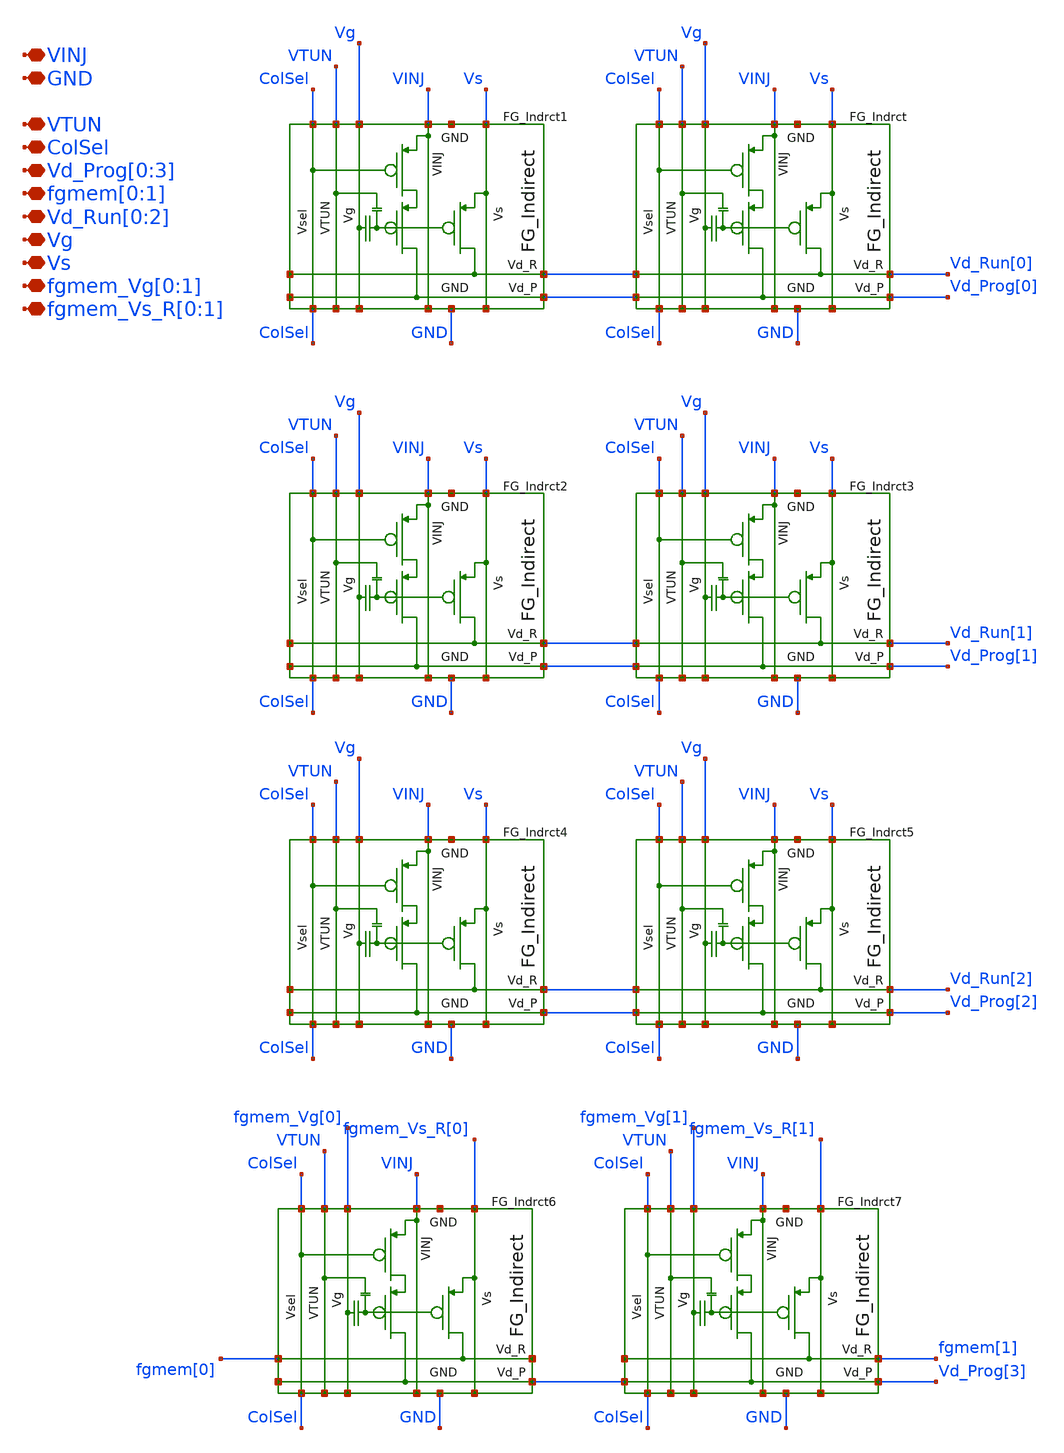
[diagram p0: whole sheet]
** sch_path: sky130_cells/IndirectVMM_Bot_Bmat_4x2/IndirectVMM_Bot_Bmat_4x2.sch
**.subckt IndirectVMM_Bot_Bmat_4x2 Vd_Run[0],Vd_Run[1],Vd_Run[2]
*+ Vd_Prog[0],Vd_Prog[1],Vd_Prog[2],Vd_Prog[3] Vg VTUN ColSel GND VINJ Vs fgmem[0],fgmem[1] fgmem_Vg[0],fgmem_Vg[1] fgmem_Vs_R[0],fgmem_Vs_R[1]
*.iopin Vd_Run[0],Vd_Run[1],Vd_Run[2]
*.iopin Vd_Prog[0],Vd_Prog[1],Vd_Prog[2],Vd_Prog[3]
*.iopin Vg
*.iopin VTUN
*.iopin ColSel
*.iopin GND
*.iopin VINJ
*.iopin Vs
*.iopin fgmem[0],fgmem[1]
*.iopin fgmem_Vg[0],fgmem_Vg[1]
*.iopin fgmem_Vs_R[0],fgmem_Vs_R[1]
FG_Indrct1 Vs Vg ColSel VTUN Vd_Run[0] Vd_Prog[0] VINJ GND FG_Indirect
FG_Indrct Vs Vg ColSel VTUN Vd_Run[0] Vd_Prog[0] VINJ GND FG_Indirect
FG_Indrct2 Vs Vg ColSel VTUN Vd_Run[1] Vd_Prog[1] VINJ GND FG_Indirect
FG_Indrct3 Vs Vg ColSel VTUN Vd_Run[1] Vd_Prog[1] VINJ GND FG_Indirect
FG_Indrct4 Vs Vg ColSel VTUN Vd_Run[2] Vd_Prog[2] VINJ GND FG_Indirect
FG_Indrct5 Vs Vg ColSel VTUN Vd_Run[2] Vd_Prog[2] VINJ GND FG_Indirect
FG_Indrct6 fgmem_Vs_R[0] fgmem_Vg[0] ColSel VTUN fgmem[0] Vd_Prog[3] VINJ GND FG_Indirect
FG_Indrct7 fgmem_Vs_R[1] fgmem_Vg[1] ColSel VTUN fgmem[1] Vd_Prog[3] VINJ GND FG_Indirect
**.ends

* expanding   symbol:  sky130_cells/Floating_Gates/Indirect/FG_Indirect.sym # of pins=16
** sym_path: sky130_cells/Floating_Gates/Indirect/FG_Indirect.sym
** sch_path: sky130_cells/Floating_Gates/Indirect/FG_Indirect.sch
.subckt FG_Indirect Vs Vg Vsel VTUN Vd_R Vd_P VINJ GND
*.iopin VINJ
*.iopin Vsel
*.iopin Vg
*.iopin Vs
*.iopin Vd_R
*.iopin Vd_P
*.iopin VTUN
*.iopin GND
XM1 Vd_R Vfg Vs VINJ sky130_fd_pr__pfet_g5v0d10v5 L=0.5 W=0.42 nf=1 ad='int((nf+1)/2) * W/nf * 0.29'
+ as='int((nf+2)/2) * W/nf * 0.29' pd='2*int((nf+1)/2) * (W/nf + 0.29)' ps='2*int((nf+2)/2) * (W/nf + 0.29)'
+ nrd='0.29 / W' nrs='0.29 / W' sa=0 sb=0 sd=0 mult=1 m=1
XM2 net1 Vsel VINJ VINJ sky130_fd_pr__pfet_g5v0d10v5 L=0.5 W=0.42 nf=1 ad='int((nf+1)/2) * W/nf * 0.29'
+ as='int((nf+2)/2) * W/nf * 0.29' pd='2*int((nf+1)/2) * (W/nf + 0.29)' ps='2*int((nf+2)/2) * (W/nf + 0.29)'
+ nrd='0.29 / W' nrs='0.29 / W' sa=0 sb=0 sd=0 mult=1 m=1
XM3 Vd_P Vfg net1 VINJ sky130_fd_pr__pfet_g5v0d10v5 L=0.5 W=0.42 nf=1 ad='int((nf+1)/2) * W/nf * 0.29'
+ as='int((nf+2)/2) * W/nf * 0.29' pd='2*int((nf+1)/2) * (W/nf + 0.29)' ps='2*int((nf+2)/2) * (W/nf + 0.29)'
+ nrd='0.29 / W' nrs='0.29 / W' sa=0 sb=0 sd=0 mult=1 m=1
XC1 Vfg VTUN GND sky130_fd_pr__cap_var_hvt W=0.29 L=0.5 VM=1 m=1
XC2 Vfg Vg GND sky130_fd_pr__cap_var_hvt W=0.54 L=0.65 VM=1 m=1
.ends

.end
